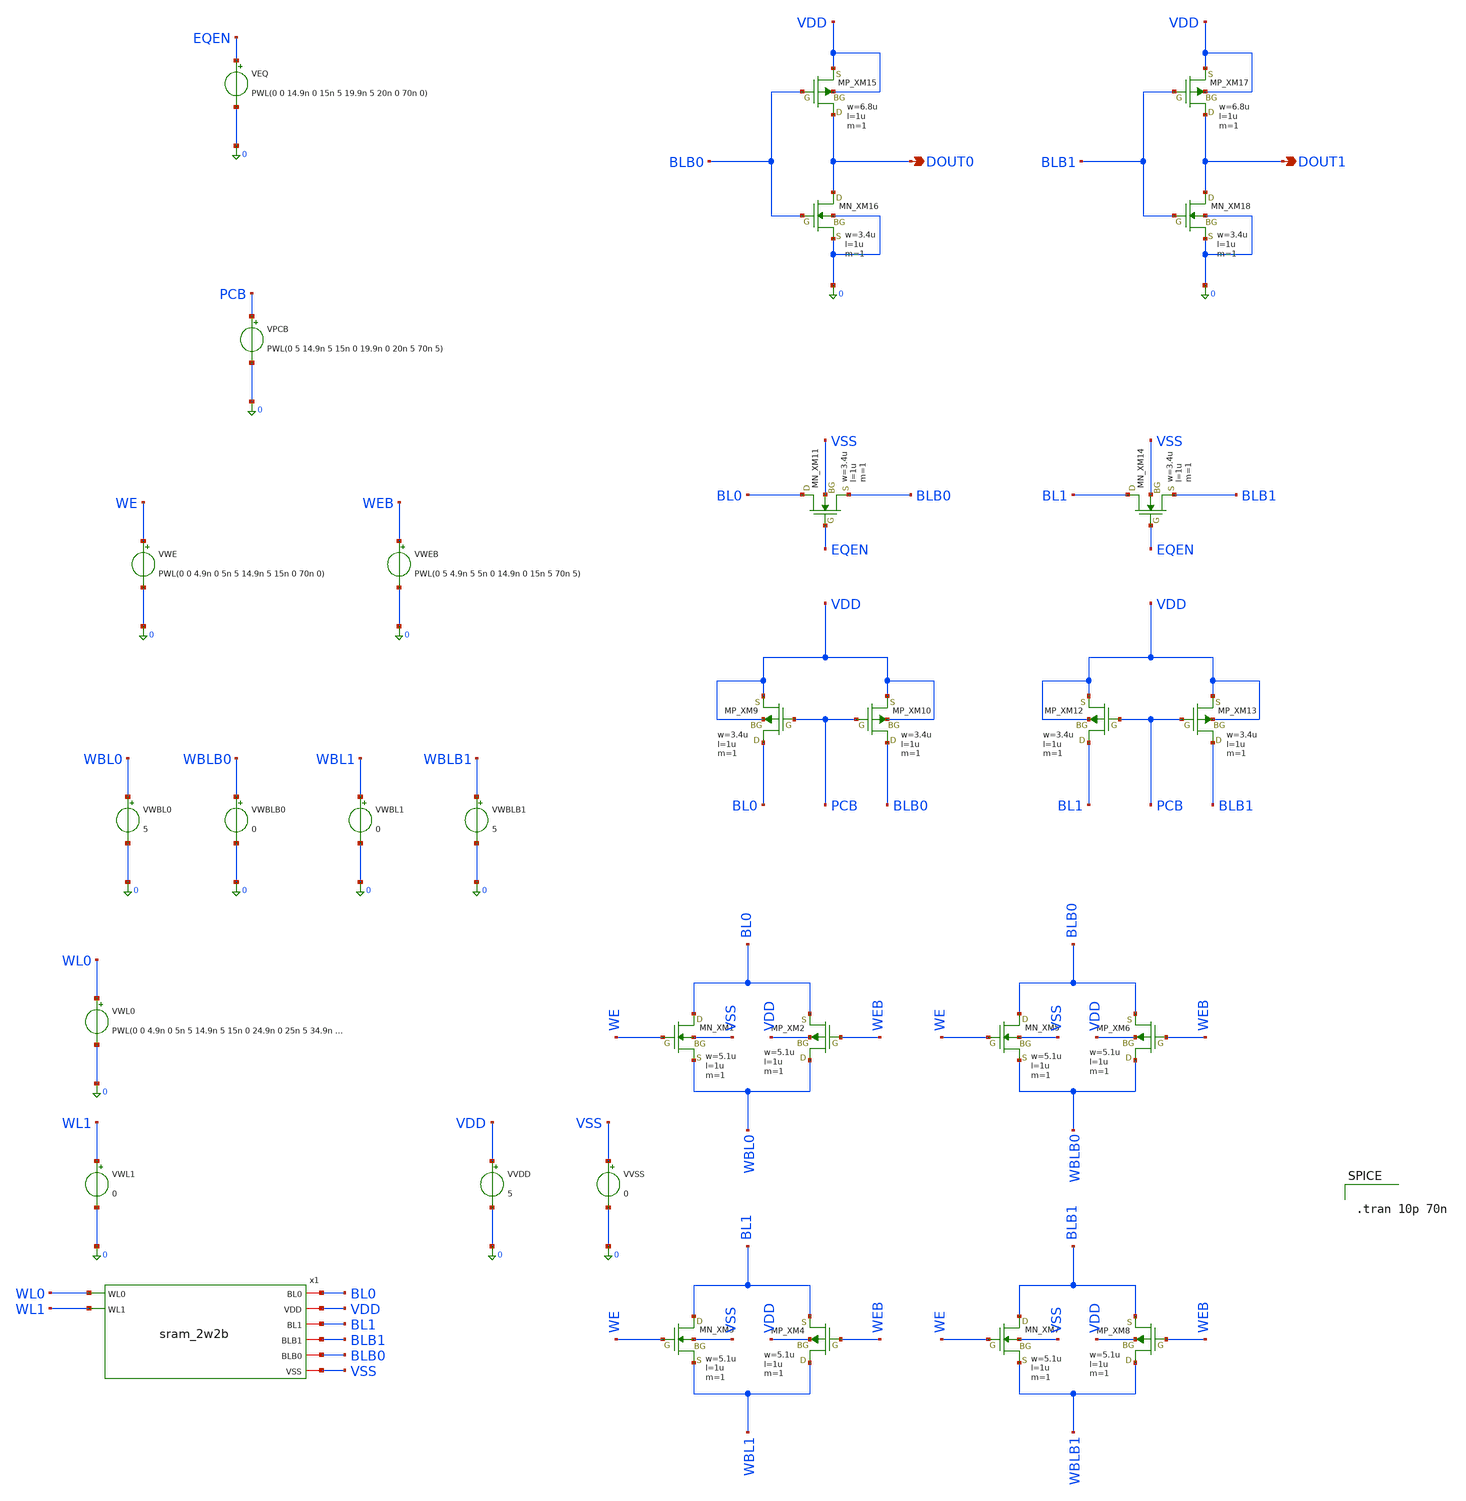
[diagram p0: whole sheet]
** sch_path: array/2word_x_2bit/tb_sram_2w2b.sch
**.subckt tb_sram_2w2b DOUT0 DOUT1
*.opin DOUT0
*.opin DOUT1
x1 WL0 BL0 VDD BL1 BLB1 WL1 BLB0 VSS sram_2w2b
VWL0 WL0 0 PWL(0 0 4.9n 0 5n 5 14.9n 5 15n 0 24.9n 0 25n 5 34.9n 5 35n 0 70n 0)
VWL1 WL1 0 0
VVDD VDD 0 5
XXM1 BL0 WE WBL0 VSS NMOS w=5.1u l=1u nrd=0 nrs=0 m=1
XXM2 WBL0 WEB BL0 VDD PMOS w=5.1u l=1u nrd=0 nrs=0 m=1
XXM5 BLB0 WE WBLB0 VSS NMOS w=5.1u l=1u nrd=0 nrs=0 m=1
XXM6 WBLB0 WEB BLB0 VDD PMOS w=5.1u l=1u nrd=0 nrs=0 m=1
XXM3 BL1 WE WBL1 VSS NMOS w=5.1u l=1u nrd=0 nrs=0 m=1
XXM4 WBL1 WEB BL1 VDD PMOS w=5.1u l=1u nrd=0 nrs=0 m=1
XXM7 BLB1 WE WBLB1 VSS NMOS w=5.1u l=1u nrd=0 nrs=0 m=1
XXM8 WBLB1 WEB BLB1 VDD PMOS w=5.1u l=1u nrd=0 nrs=0 m=1
VWBL0 WBL0 0 5
VWBLB0 WBLB0 0 0
VWBL1 WBL1 0 0
VWBLB1 WBLB1 0 5
VVSS VSS 0 0
VWE WE 0 PWL(0 0 4.9n 0 5n 5 14.9n 5 15n 0 70n 0)
VWEB WEB 0 PWL(0 5 4.9n 5 5n 0 14.9n 0 15n 5 70n 5)
XXM9 BL0 PCB VDD VDD PMOS w=3.4u l=1u nrd=0 nrs=0 m=1
XXM10 BLB0 PCB VDD VDD PMOS w=3.4u l=1u nrd=0 nrs=0 m=1
XXM11 BL0 EQEN BLB0 VSS NMOS w=3.4u l=1u nrd=0 nrs=0 m=1
XXM12 BL1 PCB VDD VDD PMOS w=3.4u l=1u nrd=0 nrs=0 m=1
XXM13 BLB1 PCB VDD VDD PMOS w=3.4u l=1u nrd=0 nrs=0 m=1
XXM14 BL1 EQEN BLB1 VSS NMOS w=3.4u l=1u nrd=0 nrs=0 m=1
XXM15 DOUT0 BLB0 VDD VDD PMOS w=6.8u l=1u nrd=0 nrs=0 m=1
XXM16 DOUT0 BLB0 0 0 NMOS w=3.4u l=1u nrd=0 nrs=0 m=1
XXM17 DOUT1 BLB1 VDD VDD PMOS w=6.8u l=1u nrd=0 nrs=0 m=1
XXM18 DOUT1 BLB1 0 0 NMOS w=3.4u l=1u nrd=0 nrs=0 m=1
VPCB PCB 0 PWL(0 5 14.9n 5 15n 0 19.9n 0 20n 5 70n 5)
VEQ EQEN 0 PWL(0 0 14.9n 0 15n 5 19.9n 5 20n 0 70n 0)
**** begin user architecture code
 .include $::LIB/ip62_models


.tran 10p 70n



**** end user architecture code
**.ends
.end
